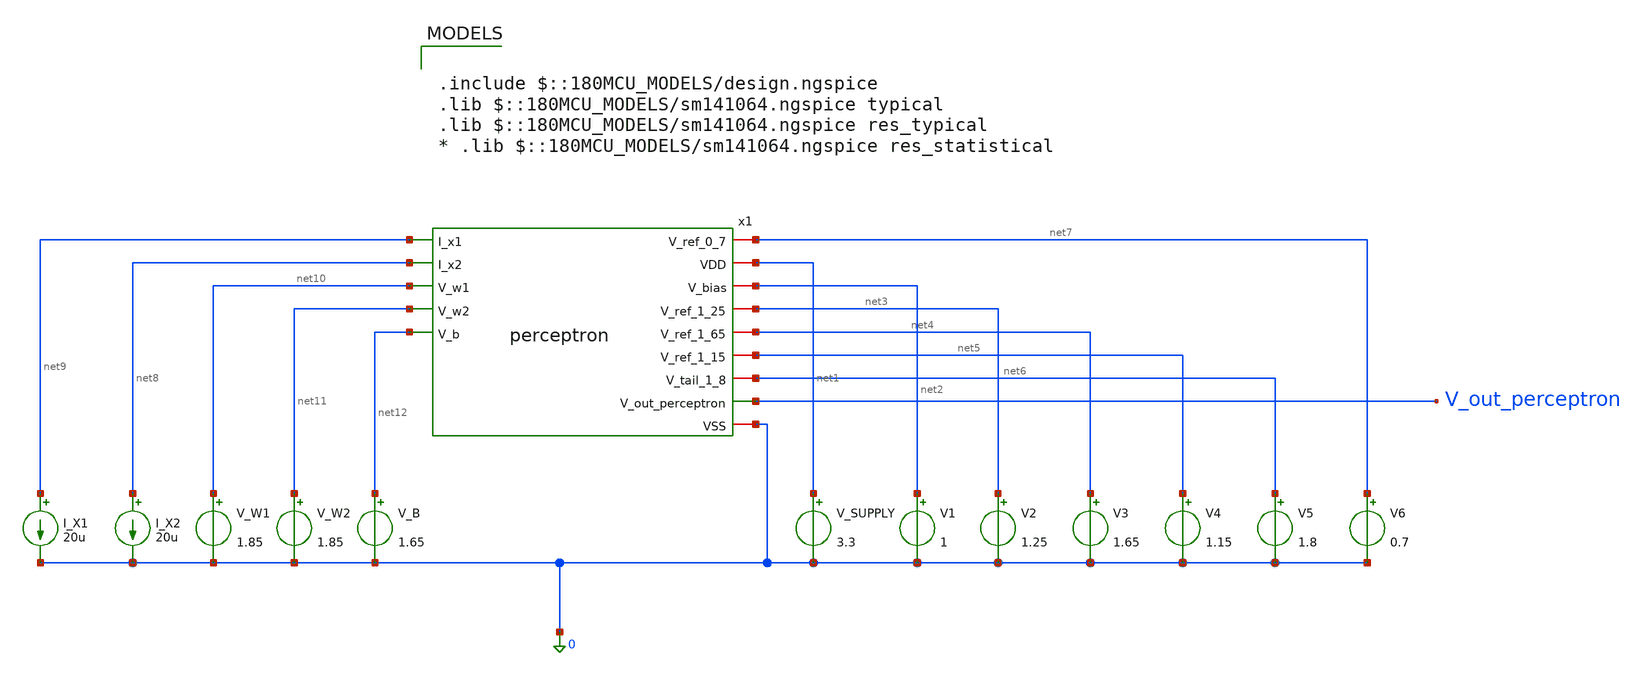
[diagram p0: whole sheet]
** sch_path: schematics/tb_perceptron.sch
**.subckt tb_perceptron
x1 net7 net1 net2 net3 net4 net5 net6 net9 net8 V_out_perceptron net10 net11 0 net12 perceptron
V_SUPPLY net1 0 3.3
V1 net2 0 1
V2 net3 0 1.25
V3 net4 0 1.65
V4 net5 0 1.15
V5 net6 0 1.8
V6 net7 0 0.7
I_X1 net9 0 20u
I_X2 net8 0 20u
V_W1 net10 0 1.85
V_W2 net11 0 1.85
V_B net12 0 1.65
**** begin user architecture code


.control
  * --- UI THEME OVERRIDES ---
  set color0=white
  set color1=black
  set xbrushwidth=2

  * ==========================================
  * GRAPH 1: Weights (Inhibitive to Excitatory)
  * ==========================================
  alter I_X2 = 0
  alter V_W2 = 1.65
  alter V_B = 1.65
  * Sweep Sensor 1, Step Weight 1 (-200mV, 0mV, +200mV)
  dc I_X1 0 50u 1u V_W1 1.45 1.85 0.2
  set title="Graph 1: Weight Sweep (Inhibitory, Neutral, Excitatory)"
  plot v(V_out_perceptron)

  * ==========================================
  * GRAPH 2: Sensor Interference
  * ==========================================
  alter V_W1 = 1.85
  alter V_W2 = 1.85
  alter V_B = 1.65
  * Both weights strongly positive. Sweep X1, Step X2 (0, 25u, 50u)
  dc I_X1 0 50u 1u I_X2 0 50u 25u
  set title="Graph 2: Sensor 1 vs Sensor 2 Interference"
  plot v(V_out_perceptron)

  * ==========================================
  * GRAPH 3: Bias Shifting
  * ==========================================
  alter I_X2 = 0
  alter V_W1 = 1.85
  * Sensor 1 sweeping, Weight 1 positive, Step Bias
  dc I_X1 0 50u 1u V_B 1.45 1.85 0.2
  set title="Graph 3: Bias shifting the S-Curve horizontally"
  plot v(V_out_perceptron)

  * ==========================================
  * 3D DATA GENERATION (Silent Export)
  * ==========================================
  * 3D Plot A: X = Sensor 1, Y = Sensor 2, Z = Output
  alter V_W1 = 1.85
  alter V_W2 = 1.85
  alter V_B = 1.65
  dc I_X1 0 50u 1u I_X2 0 50u 2u
  wrdata /foss/designs/analog-perceptron-gf180mcu/schematics/3d_sensors.txt v(V_out_perceptron)

  * 3D Plot B: X = Weight 1, Y = Weight 2, Z = Output
  alter I_X1 = 50u
  alter I_X2 = 50u
  alter V_B = 1.65
  dc V_W1 1.45 1.85 0.01 V_W2 1.45 1.85 0.02
  wrdata /foss/designs/analog-perceptron-gf180mcu/schematics/3d_weights.txt v(V_out_perceptron)
.endc



.include $::180MCU_MODELS/design.ngspice
.lib $::180MCU_MODELS/sm141064.ngspice typical
.lib $::180MCU_MODELS/sm141064.ngspice res_typical
* .lib $::180MCU_MODELS/sm141064.ngspice res_statistical

**** end user architecture code
**.ends

* expanding   symbol:  analog-perceptron-gf180mcu/schematics/perceptron.sym # of pins=14
** sym_path: schematics/perceptron.sym
** sch_path: schematics/perceptron.sch
.subckt perceptron V_ref_0_7 VDD V_bias V_ref_1_25 V_ref_1_65 V_ref_1_15 V_tail_1_8 I_x1 I_x2
+ V_out_perceptron V_w1 V_w2 VSS V_b
*.iopin VDD
*.iopin VSS
*.iopin V_bias
*.ipin I_x1
*.ipin I_x2
*.iopin V_ref_1_25
*.iopin V_ref_1_15
*.iopin V_ref_1_65
*.iopin V_tail_1_8
*.ipin V_w1
*.ipin V_w2
*.ipin V_b
*.iopin V_ref_0_7
*.opin V_out_perceptron
x1 V_ref_1_25 net4 V_bias I_x1 VSS cg_amp_tia
x2 V_ref_1_25 net3 V_bias I_x2 VSS cg_amp_tia
x_g1 net1 net2 V_w1 V_ref_1_65 V_ref_1_25 net4 V_tail_1_8 VSS gilbert_multiplier_current
x_g2 net1 net2 V_w2 V_ref_1_65 V_ref_1_25 net3 V_tail_1_8 VSS gilbert_multiplier_current
x_g3 net1 net2 V_b V_ref_1_65 V_ref_1_25 V_ref_1_15 V_tail_1_8 VSS gilbert_multiplier_current
x_tanh VDD V_ref_1_65 V_out_perceptron net1 net2 V_ref_0_7 VSS tanh_ota
XR1 net1 VDD VSS ppolyf_u r_width=1e-6 r_length=7e-6 m=1
XR2 net2 VDD VSS ppolyf_u r_width=1e-6 r_length=7e-6 m=1
.ends


* expanding   symbol:  analog-perceptron-gf180mcu/schematics/cg_amp_tia.sym # of pins=5
** sym_path: schematics/cg_amp_tia.sym
** sch_path: schematics/cg_amp_tia.sch
.subckt cg_amp_tia V_ref V_out V_bias I_in VSS
*.iopin V_ref
*.iopin VSS
*.ipin I_in
*.ipin V_bias
*.opin V_out
XM1 V_out V_bias I_in VSS nfet_03v3 L=0.5u W=5u nf=1 ad='int((nf+1)/2) * W/nf * 0.18u' as='int((nf+2)/2) * W/nf * 0.18u'
+ pd='2*int((nf+1)/2) * (W/nf + 0.18u)' ps='2*int((nf+2)/2) * (W/nf + 0.18u)' nrd='0.18u / W' nrs='0.18u / W'
+ sa=0 sb=0 sd=0 m=1
XR1 V_out V_ref VSS ppolyf_u_1k r_width=3e-6 r_length=8.1e-6 m=1
.ends


* expanding   symbol:  analog-perceptron-gf180mcu/schematics/gilbert_multiplier_current.sym # of
*+ pins=8
** sym_path: schematics/gilbert_multiplier_current.sym
** sch_path: schematics/gilbert_multiplier_current.sch
.subckt gilbert_multiplier_current I_o_p I_o_n V_w_p V_w_n V_x_p V_x_n V_tail VSS
*.ipin V_x_p
*.ipin V_x_n
*.ipin V_tail
*.iopin VSS
*.ipin V_w_p
*.ipin V_w_n
*.opin I_o_n
*.opin I_o_p
XM1 net1 V_x_p net3 VSS nfet_03v3 L=0.5u W=10u nf=1 ad='int((nf+1)/2) * W/nf * 0.18u' as='int((nf+2)/2) * W/nf * 0.18u'
+ pd='2*int((nf+1)/2) * (W/nf + 0.18u)' ps='2*int((nf+2)/2) * (W/nf + 0.18u)' nrd='0.18u / W' nrs='0.18u / W'
+ sa=0 sb=0 sd=0 m=1
XM2 net2 V_x_n net4 VSS nfet_03v3 L=0.5u W=10u nf=1 ad='int((nf+1)/2) * W/nf * 0.18u' as='int((nf+2)/2) * W/nf * 0.18u'
+ pd='2*int((nf+1)/2) * (W/nf + 0.18u)' ps='2*int((nf+2)/2) * (W/nf + 0.18u)' nrd='0.18u / W' nrs='0.18u / W'
+ sa=0 sb=0 sd=0 m=1
XM3 I_o_n V_w_p net1 VSS nfet_03v3 L=0.5u W=10u nf=1 ad='int((nf+1)/2) * W/nf * 0.18u' as='int((nf+2)/2) * W/nf * 0.18u'
+ pd='2*int((nf+1)/2) * (W/nf + 0.18u)' ps='2*int((nf+2)/2) * (W/nf + 0.18u)' nrd='0.18u / W' nrs='0.18u / W'
+ sa=0 sb=0 sd=0 m=1
XM4 I_o_p V_w_n net1 VSS nfet_03v3 L=0.5u W=10u nf=1 ad='int((nf+1)/2) * W/nf * 0.18u' as='int((nf+2)/2) * W/nf * 0.18u'
+ pd='2*int((nf+1)/2) * (W/nf + 0.18u)' ps='2*int((nf+2)/2) * (W/nf + 0.18u)' nrd='0.18u / W' nrs='0.18u / W'
+ sa=0 sb=0 sd=0 m=1
XM5 I_o_n V_w_n net2 VSS nfet_03v3 L=0.5u W=10u nf=1 ad='int((nf+1)/2) * W/nf * 0.18u' as='int((nf+2)/2) * W/nf * 0.18u'
+ pd='2*int((nf+1)/2) * (W/nf + 0.18u)' ps='2*int((nf+2)/2) * (W/nf + 0.18u)' nrd='0.18u / W' nrs='0.18u / W'
+ sa=0 sb=0 sd=0 m=1
XM6 I_o_p V_w_p net2 VSS nfet_03v3 L=0.5u W=10u nf=1 ad='int((nf+1)/2) * W/nf * 0.18u' as='int((nf+2)/2) * W/nf * 0.18u'
+ pd='2*int((nf+1)/2) * (W/nf + 0.18u)' ps='2*int((nf+2)/2) * (W/nf + 0.18u)' nrd='0.18u / W' nrs='0.18u / W'
+ sa=0 sb=0 sd=0 m=1
XM7 net3 V_tail VSS VSS nfet_03v3 L=1u W=5u nf=1 ad='int((nf+1)/2) * W/nf * 0.18u' as='int((nf+2)/2) * W/nf * 0.18u'
+ pd='2*int((nf+1)/2) * (W/nf + 0.18u)' ps='2*int((nf+2)/2) * (W/nf + 0.18u)' nrd='0.18u / W' nrs='0.18u / W'
+ sa=0 sb=0 sd=0 m=1
XM8 net4 V_tail VSS VSS nfet_03v3 L=1u W=5u nf=1 ad='int((nf+1)/2) * W/nf * 0.18u' as='int((nf+2)/2) * W/nf * 0.18u'
+ pd='2*int((nf+1)/2) * (W/nf + 0.18u)' ps='2*int((nf+2)/2) * (W/nf + 0.18u)' nrd='0.18u / W' nrs='0.18u / W'
+ sa=0 sb=0 sd=0 m=1
XR1 net3 net4 VSS ppolyf_u_1k r_width=3e-6 r_length=46.2e-6 m=1
.ends


* expanding   symbol:  analog-perceptron-gf180mcu/schematics/tanh_ota.sym # of pins=7
** sym_path: schematics/tanh_ota.sym
** sch_path: schematics/tanh_ota.sch
.subckt tanh_ota VDD V_ref V_out V_in_p V_in_n V_bias VSS
*.iopin VDD
*.iopin VSS
*.ipin V_in_p
*.ipin V_in_n
*.ipin V_bias
*.opin V_out
*.iopin V_ref
XM1 net2 V_in_p net1 VSS nfet_03v3 L=0.5u W=10u nf=1 ad='int((nf+1)/2) * W/nf * 0.18u' as='int((nf+2)/2) * W/nf * 0.18u'
+ pd='2*int((nf+1)/2) * (W/nf + 0.18u)' ps='2*int((nf+2)/2) * (W/nf + 0.18u)' nrd='0.18u / W' nrs='0.18u / W'
+ sa=0 sb=0 sd=0 m=1
XM2 V_out V_in_n net1 VSS nfet_03v3 L=0.5u W=10u nf=1 ad='int((nf+1)/2) * W/nf * 0.18u' as='int((nf+2)/2) * W/nf * 0.18u'
+ pd='2*int((nf+1)/2) * (W/nf + 0.18u)' ps='2*int((nf+2)/2) * (W/nf + 0.18u)' nrd='0.18u / W' nrs='0.18u / W'
+ sa=0 sb=0 sd=0 m=1
XM3 net1 V_bias VSS VSS nfet_03v3 L=0.5u W=10u nf=1 ad='int((nf+1)/2) * W/nf * 0.18u' as='int((nf+2)/2) * W/nf * 0.18u'
+ pd='2*int((nf+1)/2) * (W/nf + 0.18u)' ps='2*int((nf+2)/2) * (W/nf + 0.18u)' nrd='0.18u / W' nrs='0.18u / W'
+ sa=0 sb=0 sd=0 m=1
XM4 net2 net2 VDD VDD pfet_03v3 L=0.5u W=20u nf=1 ad='int((nf+1)/2) * W/nf * 0.18u' as='int((nf+2)/2) * W/nf * 0.18u'
+ pd='2*int((nf+1)/2) * (W/nf + 0.18u)' ps='2*int((nf+2)/2) * (W/nf + 0.18u)' nrd='0.18u / W' nrs='0.18u / W'
+ sa=0 sb=0 sd=0 m=1
XM5 V_out net2 VDD VDD pfet_03v3 L=0.5u W=20u nf=1 ad='int((nf+1)/2) * W/nf * 0.18u' as='int((nf+2)/2) * W/nf * 0.18u'
+ pd='2*int((nf+1)/2) * (W/nf + 0.18u)' ps='2*int((nf+2)/2) * (W/nf + 0.18u)' nrd='0.18u / W' nrs='0.18u / W'
+ sa=0 sb=0 sd=0 m=1
XR1 net3 V_ref VSS ppolyf_u_1k r_width=3e-6 r_length=12.4e-6 m=1
XR2 net4 net3 VSS ppolyf_u_1k r_width=3e-6 r_length=12.4e-6 m=1
XR3 net5 net4 VSS ppolyf_u_1k r_width=3e-6 r_length=12.4e-6 m=1
XR4 net6 net5 VSS ppolyf_u_1k r_width=3e-6 r_length=12.4e-6 m=1
XR5 net7 net6 VSS ppolyf_u_1k r_width=3e-6 r_length=12.4e-6 m=1
XR6 V_out net7 VSS ppolyf_u_1k r_width=3e-6 r_length=12.4e-6 m=1
.ends

.end
